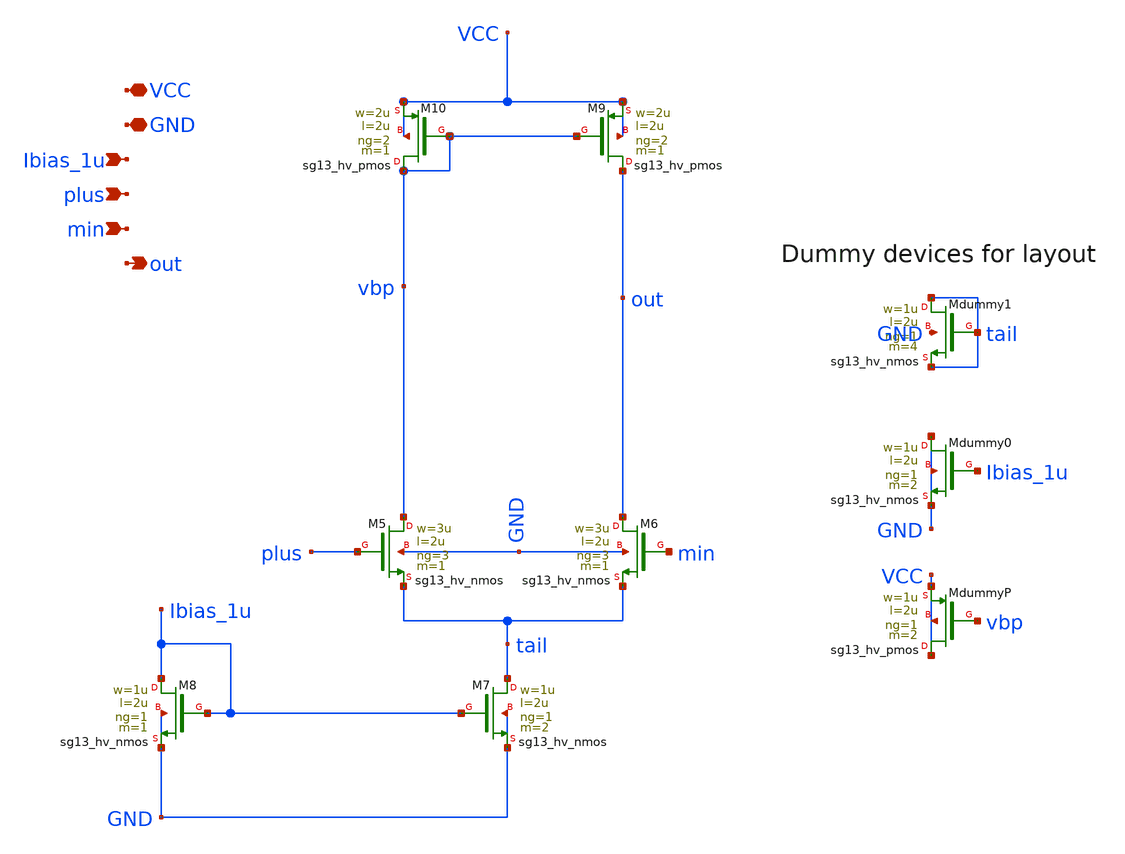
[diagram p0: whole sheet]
** sch_path: FLDO/design_data/xschem/ldo_ota.sch
**.subckt ldo_ota VCC GND plus min out Ibias_1u
*.iopin VCC
*.iopin GND
*.ipin plus
*.ipin min
*.opin out
*.ipin Ibias_1u
XM5 vbp plus tail GND sg13_hv_nmos w=3u l=2u ng=3 m=1 mm_ok=1
XM6 out min tail GND sg13_hv_nmos w=3u l=2u ng=3 m=1 mm_ok=1
XM7 tail Ibias_1u GND GND sg13_hv_nmos w=1u l=2u ng=1 m=2 mm_ok=1
XM8 Ibias_1u Ibias_1u GND GND sg13_hv_nmos w=1u l=2u ng=1 m=1 mm_ok=1
XM9 out vbp VCC VCC sg13_hv_pmos w=2u l=2u ng=2 m=1 mm_ok=1
XM10 vbp vbp VCC VCC sg13_hv_pmos w=2u l=2u ng=2 m=1 mm_ok=1
XMdummy0 GND Ibias_1u GND GND sg13_hv_nmos w=1u l=2u ng=1 m=2 mm_ok=1
XMdummy1 tail tail tail GND sg13_hv_nmos w=1u l=2u ng=1 m=4 mm_ok=1
XMdummyP VCC vbp VCC VCC sg13_hv_pmos w=1u l=2u ng=1 m=2 mm_ok=1
**.ends
.end
